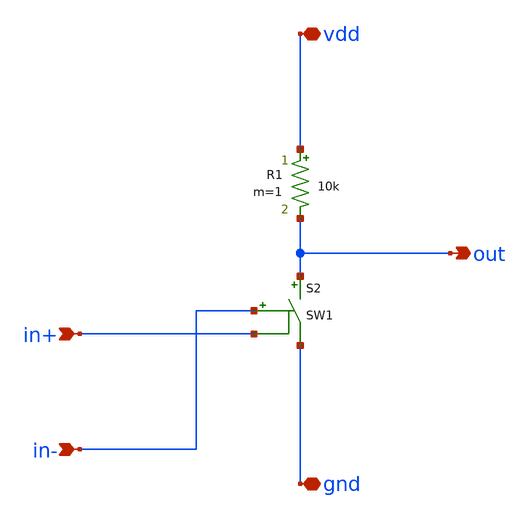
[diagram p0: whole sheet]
** sch_path: ideal_comparator.sch
**.subckt ideal_comparator vdd gnd in+ in- out
*.iopin vdd
*.iopin gnd
*.ipin in+
*.ipin in-
*.opin out
R1 vdd out 10k m=1
S2 out gnd in- in+ SW1
**.ends
**** begin user architecture code
.MODEL SW1 SW( VT=0 VH=0.00001 RON=0.0001 ROFF=1000G )
**** end user architecture code
.end
